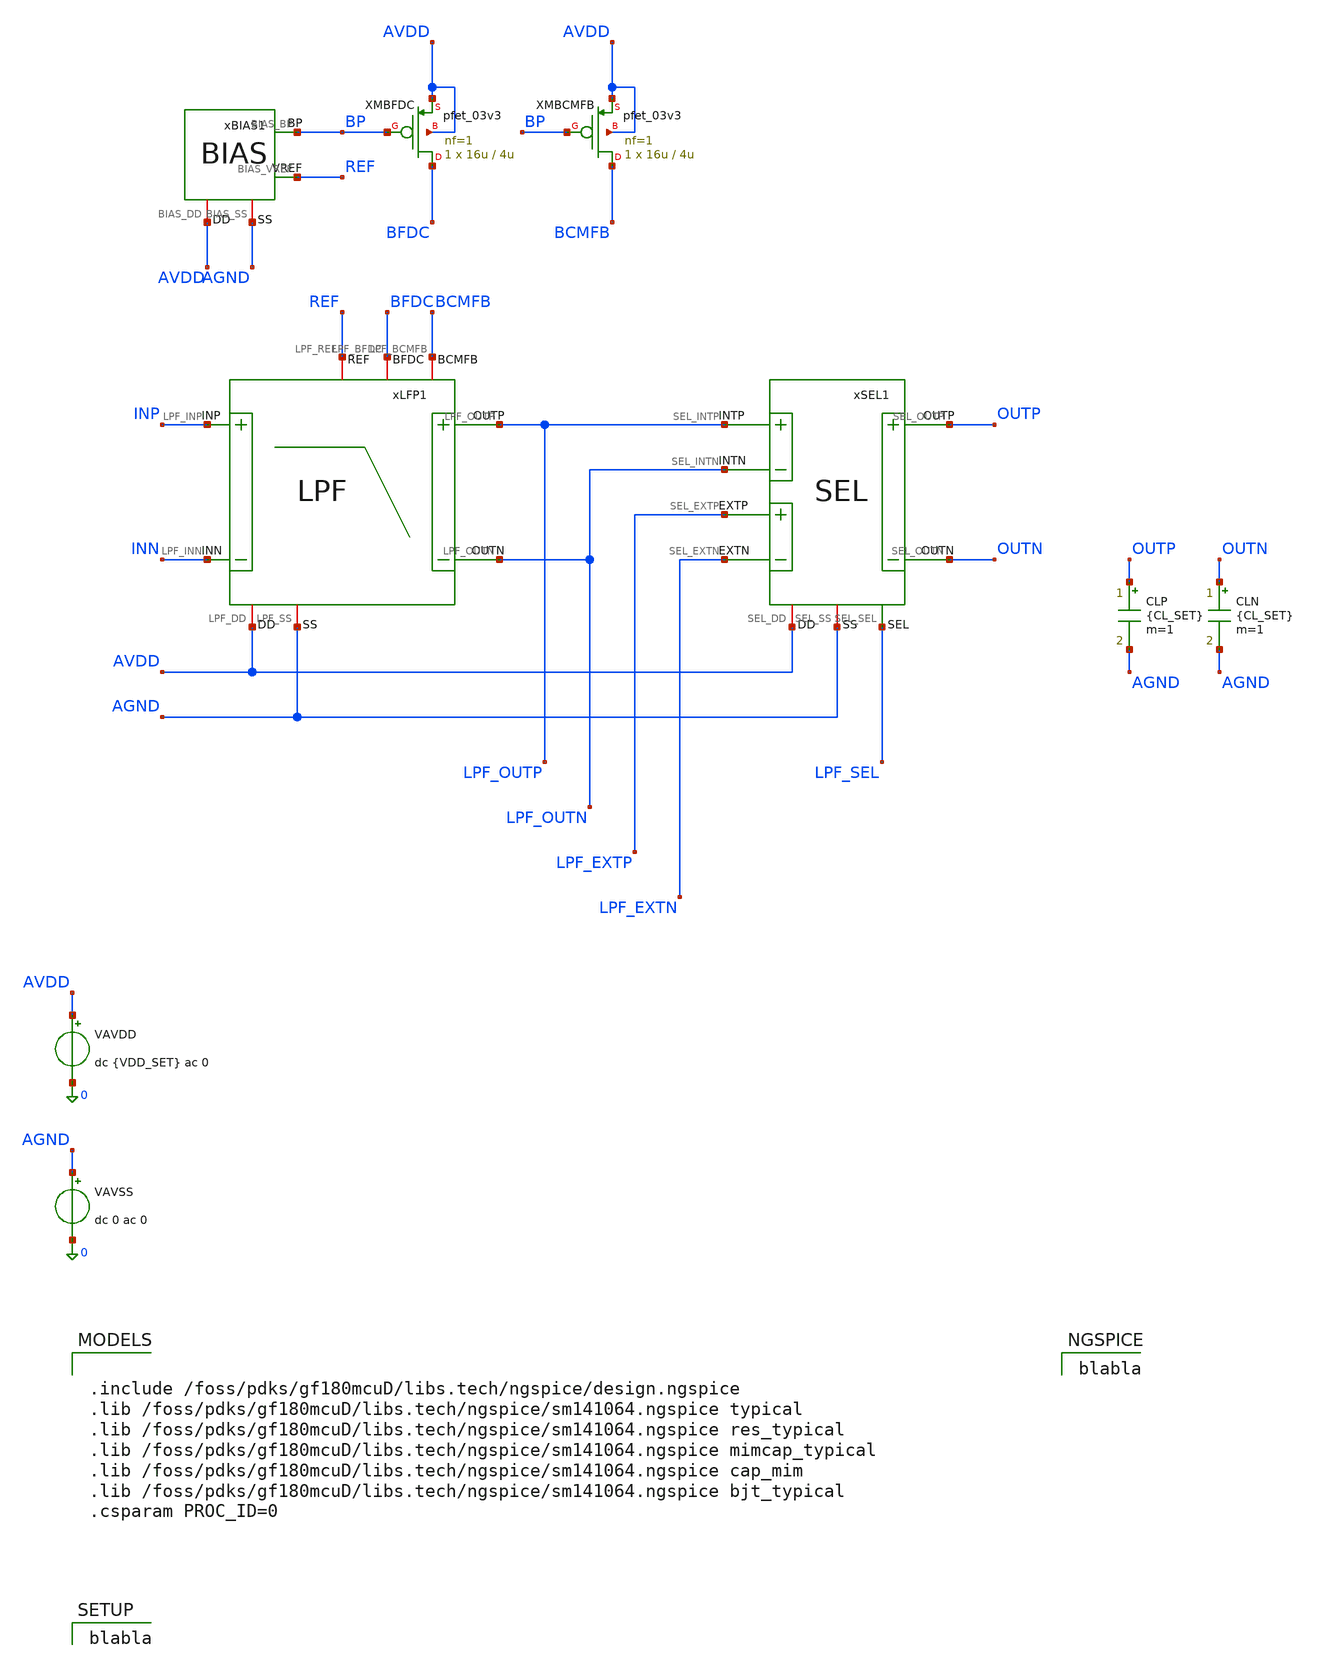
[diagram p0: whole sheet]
** sch_path: Design_Files/IC Design/Testbench/LPF/LPF_TB_NOM.sch
**.subckt LPF_TB_NOM
CLP OUTP AGND {CL_SET} m=1
CLN OUTN AGND {CL_SET} m=1
xBIAS1 AVDD AGND BP REF BIAS
XMBFDC BFDC BP AVDD AVDD pfet_03v3 L=4u W=16u nf=1 ad='int((nf+1)/2) * W/nf * 0.18u' as='int((nf+2)/2) * W/nf * 0.18u'
+ pd='2*int((nf+1)/2) * (W/nf + 0.18u)' ps='2*int((nf+2)/2) * (W/nf + 0.18u)' nrd='0.18u / W' nrs='0.18u / W'
+ sa=0 sb=0 sd=0 m=1
XMBCMFB BCMFB BP AVDD AVDD pfet_03v3 L=4u W=16u nf=1 ad='int((nf+1)/2) * W/nf * 0.18u' as='int((nf+2)/2) * W/nf * 0.18u'
+ pd='2*int((nf+1)/2) * (W/nf + 0.18u)' ps='2*int((nf+2)/2) * (W/nf + 0.18u)' nrd='0.18u / W' nrs='0.18u / W'
+ sa=0 sb=0 sd=0 m=1
VAVDD AVDD 0 dc {VDD_SET} ac 0
.save i(vavdd)
VAVSS AGND 0 dc 0 ac 0
xLFP1 AVDD AGND INP INN LPF_OUTN BFDC LPF_OUTP BCMFB REF LPF
xSEL1 AVDD AGND LPF_OUTP LPF_OUTN OUTN OUTP LPF_EXTP LPF_EXTN LPF_SEL SEL
**** begin user architecture code


.include /foss/pdks/gf180mcuD/libs.tech/ngspice/design.ngspice
.lib /foss/pdks/gf180mcuD/libs.tech/ngspice/sm141064.ngspice typical
.lib /foss/pdks/gf180mcuD/libs.tech/ngspice/sm141064.ngspice res_typical
.lib /foss/pdks/gf180mcuD/libs.tech/ngspice/sm141064.ngspice mimcap_typical
.lib /foss/pdks/gf180mcuD/libs.tech/ngspice/sm141064.ngspice cap_mim
.lib /foss/pdks/gf180mcuD/libs.tech/ngspice/sm141064.ngspice bjt_typical
.csparam PROC_ID=0



blabla


blabla

**** end user architecture code
**.ends
.end
